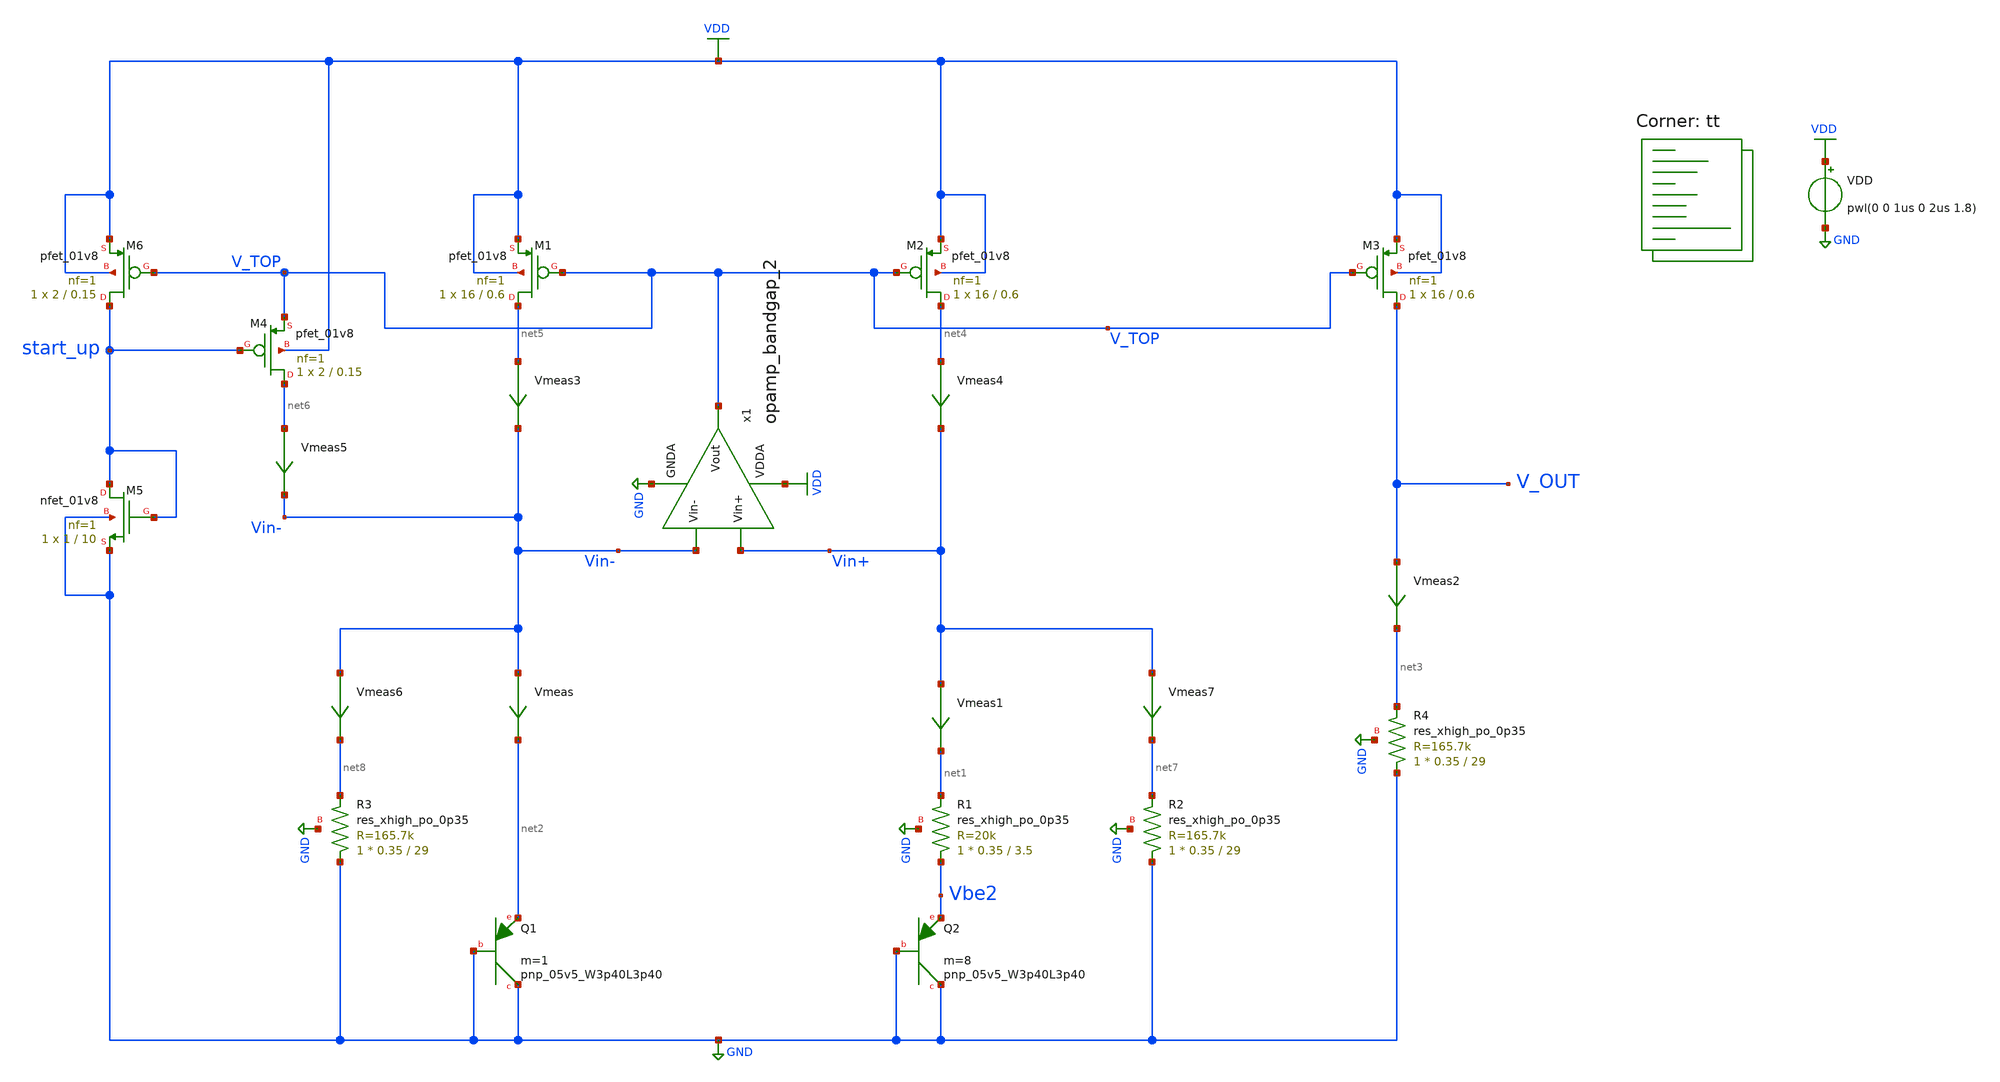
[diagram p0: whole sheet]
** sch_path: projects/bandgapref/xschem_ngspice/new_files/tb_low_voltage_BGR_2.sch
**.subckt tb_low_voltage_BGR_2
VDD VDD GND pwl(0 0 1us 0 2us 1.8)
XQ1 GND GND net2 sky130_fd_pr__pnp_05v5_W3p40L3p40 m=1
XQ2 GND GND Vbe2 sky130_fd_pr__pnp_05v5_W3p40L3p40 m=8
XM1 net5 V_TOP VDD VDD sky130_fd_pr__pfet_01v8 L=0.6 W=16 nf=1 ad='int((nf+1)/2) * W/nf * 0.29' as='int((nf+2)/2) * W/nf * 0.29'
+ pd='2*int((nf+1)/2) * (W/nf + 0.29)' ps='2*int((nf+2)/2) * (W/nf + 0.29)' nrd='0.29 / W' nrs='0.29 / W'
+ sa=0 sb=0 sd=0 mult=1 m=1
XM2 net4 V_TOP VDD VDD sky130_fd_pr__pfet_01v8 L=0.6 W=16 nf=1 ad='int((nf+1)/2) * W/nf * 0.29' as='int((nf+2)/2) * W/nf * 0.29'
+ pd='2*int((nf+1)/2) * (W/nf + 0.29)' ps='2*int((nf+2)/2) * (W/nf + 0.29)' nrd='0.29 / W' nrs='0.29 / W'
+ sa=0 sb=0 sd=0 mult=1 m=1
XM3 V_OUT V_TOP VDD VDD sky130_fd_pr__pfet_01v8 L=0.6 W=16 nf=1 ad='int((nf+1)/2) * W/nf * 0.29' as='int((nf+2)/2) * W/nf * 0.29'
+ pd='2*int((nf+1)/2) * (W/nf + 0.29)' ps='2*int((nf+2)/2) * (W/nf + 0.29)' nrd='0.29 / W' nrs='0.29 / W'
+ sa=0 sb=0 sd=0 mult=1 m=1
Vmeas Vin- net2 0
.save i(vmeas)
Vmeas1 Vin+ net1 0
.save i(vmeas1)
Vmeas2 V_OUT net3 0
.save i(vmeas2)
XR1 Vbe2 net1 GND sky130_fd_pr__res_xhigh_po_0p35 L=3.5 mult=1 m=1
XR2 GND net7 GND sky130_fd_pr__res_xhigh_po_0p35 L=29 mult=1 m=1
XR3 GND net8 GND sky130_fd_pr__res_xhigh_po_0p35 L=29 mult=1 m=1
XR4 GND net3 GND sky130_fd_pr__res_xhigh_po_0p35 L=29 mult=1 m=1
Vmeas3 net5 Vin- 0
.save i(vmeas3)
Vmeas4 net4 Vin+ 0
.save i(vmeas4)
XM5 start_up start_up GND GND sky130_fd_pr__nfet_01v8 L=10 W=1 nf=1 ad='int((nf+1)/2) * W/nf * 0.29'
+ as='int((nf+2)/2) * W/nf * 0.29' pd='2*int((nf+1)/2) * (W/nf + 0.29)' ps='2*int((nf+2)/2) * (W/nf + 0.29)'
+ nrd='0.29 / W' nrs='0.29 / W' sa=0 sb=0 sd=0 mult=1 m=1
XM6 start_up V_TOP VDD VDD sky130_fd_pr__pfet_01v8 L=0.15 W=2 nf=1 ad='int((nf+1)/2) * W/nf * 0.29' as='int((nf+2)/2) * W/nf * 0.29'
+ pd='2*int((nf+1)/2) * (W/nf + 0.29)' ps='2*int((nf+2)/2) * (W/nf + 0.29)' nrd='0.29 / W' nrs='0.29 / W'
+ sa=0 sb=0 sd=0 mult=1 m=1
Vmeas5 net6 Vin- 0
.save i(vmeas5)
XM4 net6 start_up V_TOP VDD sky130_fd_pr__pfet_01v8 L=0.15 W=2 nf=1 ad='int((nf+1)/2) * W/nf * 0.29'
+ as='int((nf+2)/2) * W/nf * 0.29' pd='2*int((nf+1)/2) * (W/nf + 0.29)' ps='2*int((nf+2)/2) * (W/nf + 0.29)'
+ nrd='0.29 / W' nrs='0.29 / W' sa=0 sb=0 sd=0 mult=1 m=1
Vmeas6 Vin- net8 0
.save i(vmeas6)
Vmeas7 Vin+ net7 0
.save i(vmeas7)
x1 VDD V_TOP Vin- Vin+ GND opamp_bandgap_2
**** begin user architecture code
.lib $::SKYWATER_MODELS/sky130.lib.spice tt



.option wnflag=1
.option savecurrents

.save @m.xm1.msky130_fd_pr__nfet_01v8[gm] @m.xm2.msky130_fd_pr__nfet_01v8[gm] @m.xm3.msky130_fd_pr__nfet_01v8[gm] @m.xm4.msky130_fd_pr__pfet_01v8[gm] @m.xm5.msky130_fd_pr__pfet_01v8[gm] @m.xm6.msky130_fd_pr__nfet_01v8[gm] @m.xm7.msky130_fd_pr__pfet_01v8[gm]

.control

  save all
   tran 1u 3m
   * ac dec 20 1 1T

  write tb_opamp_bandgap_2.raw
  set appendwrite

.endc



**** end user architecture code
**.ends

* expanding   symbol:  opamp_bandgap_2.sym # of pins=5
** sym_path: projects/bandgapref/xschem_ngspice/new_files/opamp_bandgap_2.sym
** sch_path: projects/bandgapref/xschem_ngspice/new_files/opamp_bandgap_2.sch
.subckt opamp_bandgap_2 VDDA Vout Vin- Vin+ GNDA
*.ipin Vin+
*.opin Vout
*.ipin Vin-
*.ipin GNDA
*.ipin VDDA
XM1 V_p V_mirror GNDA GNDA sky130_fd_pr__nfet_01v8 L=10 W=10 nf=1 ad='int((nf+1)/2) * W/nf * 0.29' as='int((nf+2)/2) * W/nf * 0.29'
+ pd='2*int((nf+1)/2) * (W/nf + 0.29)' ps='2*int((nf+2)/2) * (W/nf + 0.29)' nrd='0.29 / W' nrs='0.29 / W'
+ sa=0 sb=0 sd=0 mult=1 m=1
XM2 V_mirror Vin- V_p GNDA sky130_fd_pr__nfet_01v8 L=1.2 W=10 nf=1 ad='int((nf+1)/2) * W/nf * 0.29' as='int((nf+2)/2) * W/nf * 0.29'
+ pd='2*int((nf+1)/2) * (W/nf + 0.29)' ps='2*int((nf+2)/2) * (W/nf + 0.29)' nrd='0.29 / W' nrs='0.29 / W'
+ sa=0 sb=0 sd=0 mult=1 m=1
XM3 1st_Vout Vin+ V_p GNDA sky130_fd_pr__nfet_01v8 L=1.2 W=10 nf=1 ad='int((nf+1)/2) * W/nf * 0.29' as='int((nf+2)/2) * W/nf * 0.29'
+ pd='2*int((nf+1)/2) * (W/nf + 0.29)' ps='2*int((nf+2)/2) * (W/nf + 0.29)' nrd='0.29 / W' nrs='0.29 / W'
+ sa=0 sb=0 sd=0 mult=1 m=1
XM4 V_mirror V_mirror VDDA VDDA sky130_fd_pr__pfet_01v8 L=1.2 W=20 nf=2 ad='int((nf+1)/2) * W/nf * 0.29'
+ as='int((nf+2)/2) * W/nf * 0.29' pd='2*int((nf+1)/2) * (W/nf + 0.29)' ps='2*int((nf+2)/2) * (W/nf + 0.29)'
+ nrd='0.29 / W' nrs='0.29 / W' sa=0 sb=0 sd=0 mult=1 m=1
XM5 1st_Vout V_mirror VDDA VDDA sky130_fd_pr__pfet_01v8 L=1.2 W=20 nf=2 ad='int((nf+1)/2) * W/nf * 0.29'
+ as='int((nf+2)/2) * W/nf * 0.29' pd='2*int((nf+1)/2) * (W/nf + 0.29)' ps='2*int((nf+2)/2) * (W/nf + 0.29)'
+ nrd='0.29 / W' nrs='0.29 / W' sa=0 sb=0 sd=0 mult=1 m=1
XM6 Vout V_mirror GNDA GNDA sky130_fd_pr__nfet_01v8 L=10 W=10 nf=1 ad='int((nf+1)/2) * W/nf * 0.29' as='int((nf+2)/2) * W/nf * 0.29'
+ pd='2*int((nf+1)/2) * (W/nf + 0.29)' ps='2*int((nf+2)/2) * (W/nf + 0.29)' nrd='0.29 / W' nrs='0.29 / W'
+ sa=0 sb=0 sd=0 mult=1 m=1
XM7 Vout 1st_Vout VDDA VDDA sky130_fd_pr__pfet_01v8 L=1.2 W=20 nf=2 ad='int((nf+1)/2) * W/nf * 0.29'
+ as='int((nf+2)/2) * W/nf * 0.29' pd='2*int((nf+1)/2) * (W/nf + 0.29)' ps='2*int((nf+2)/2) * (W/nf + 0.29)'
+ nrd='0.29 / W' nrs='0.29 / W' sa=0 sb=0 sd=0 mult=1 m=1
.ends

.GLOBAL GND
.GLOBAL VDD
.end
